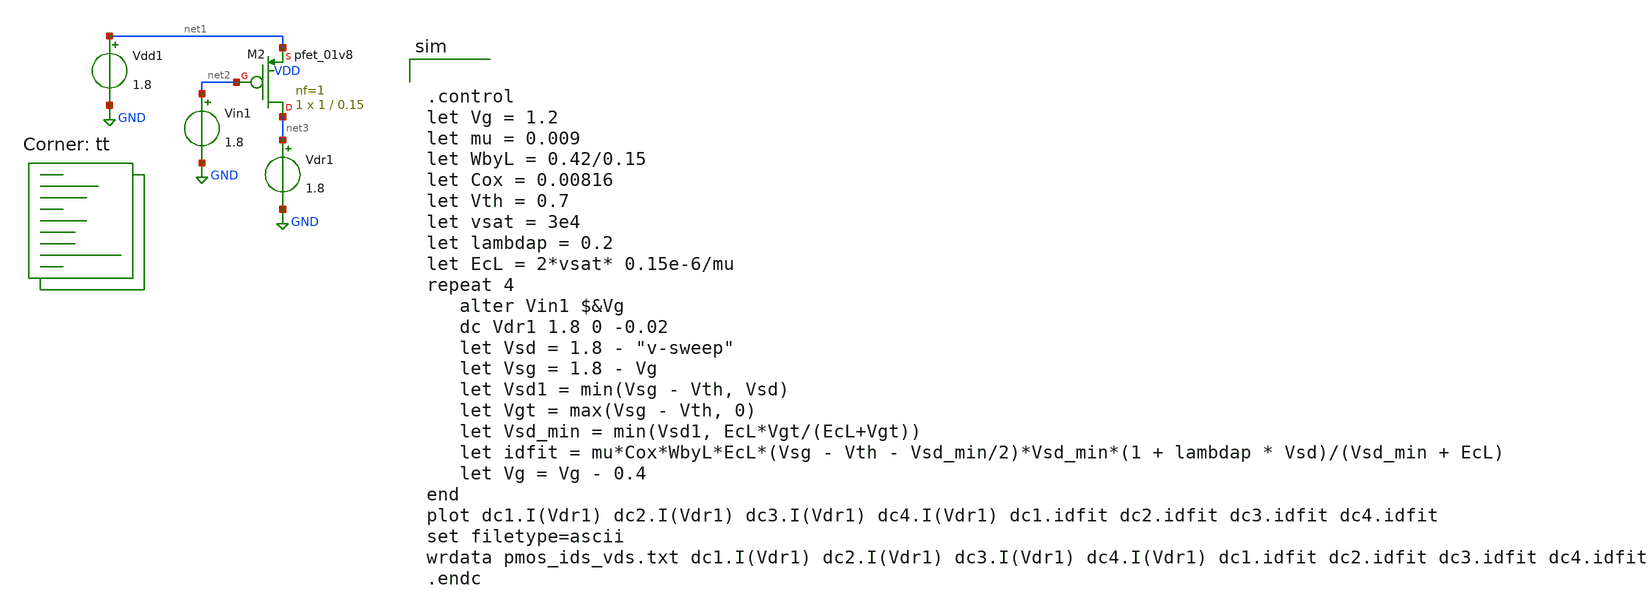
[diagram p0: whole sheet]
** sch_path: tutorial_2/tutorial_2_2b.sch
**.subckt tutorial_2_2b
XM2 net3 net2 net1 VDD sky130_fd_pr__pfet_01v8 L=0.15 W=1 nf=1 ad='int((nf+1)/2) * W/nf * 0.29' as='int((nf+2)/2) * W/nf * 0.29'
+ pd='2*int((nf+1)/2) * (W/nf + 0.29)' ps='2*int((nf+2)/2) * (W/nf + 0.29)' nrd='0.29 / W' nrs='0.29 / W'
+ sa=0 sb=0 sd=0 mult=1 m=1
Vdd1 net1 GND 1.8
Vin1 net2 GND 1.8
Vdr1 net3 GND 1.8
**** begin user architecture code


.control
let Vg = 1.2
let mu = 0.009
let WbyL = 0.42/0.15
let Cox = 0.00816
let Vth = 0.7
let vsat = 3e4
let lambdap = 0.2
let EcL = 2*vsat* 0.15e-6/mu
repeat 4
   alter Vin1 $&Vg
   dc Vdr1 1.8 0 -0.02
   let Vsd = 1.8 - "v-sweep"
   let Vsg = 1.8 - Vg
   let Vsd1 = min(Vsg - Vth, Vsd)
   let Vgt = max(Vsg - Vth, 0)
   let Vsd_min = min(Vsd1, EcL*Vgt/(EcL+Vgt))
   let idfit = mu*Cox*WbyL*EcL*(Vsg - Vth - Vsd_min/2)*Vsd_min*(1 + lambdap * Vsd)/(Vsd_min + EcL)
   let Vg = Vg - 0.4
end
plot dc1.I(Vdr1) dc2.I(Vdr1) dc3.I(Vdr1) dc4.I(Vdr1) dc1.idfit dc2.idfit dc3.idfit dc4.idfit
set filetype=ascii
wrdata pmos_ids_vds.txt dc1.I(Vdr1) dc2.I(Vdr1) dc3.I(Vdr1) dc4.I(Vdr1) dc1.idfit dc2.idfit
+ dc3.idfit dc4.idfit
.endc

.lib $::SKYWATER_MODELS/sky130.lib.spice tt
**** end user architecture code
**.ends
.GLOBAL GND
.end
